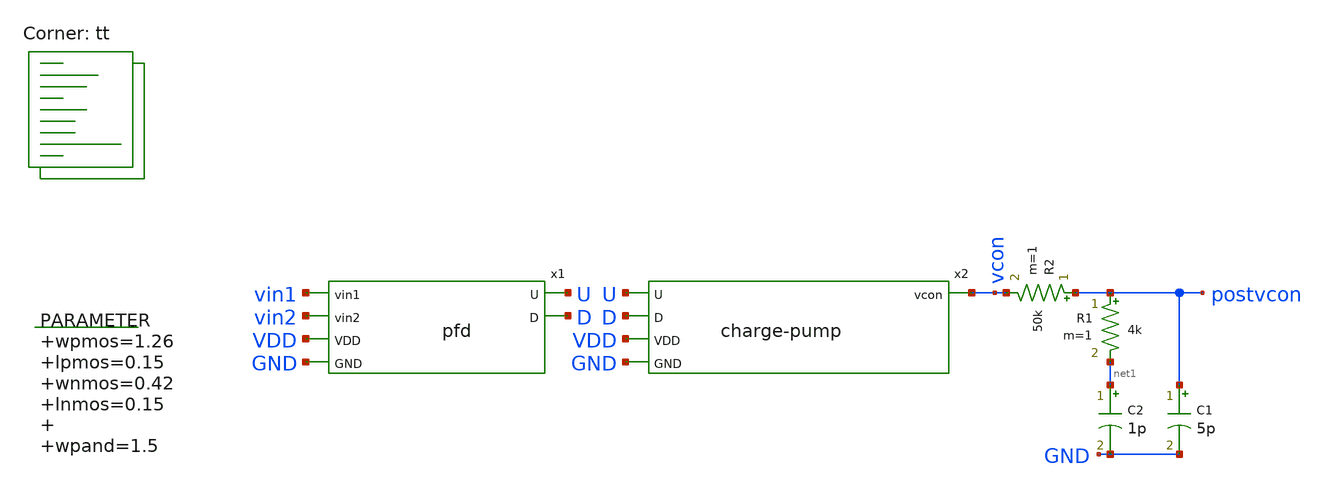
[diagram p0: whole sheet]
** sch_path: xschem/pll-tb.sch
**.subckt pll-tb
.param wpmos=1.26 lpmos=0.15 wnmos=0.42 lnmos=0.15 wpand=1.5

x2 U D vcon VDD GND charge-pump
x1 vin1 vin2 U D VDD GND pfd
C2 net1 GND 1p m=1
R1 postvcon net1 4k m=1
R2 postvcon vcon 50k m=1
C1 postvcon GND 5p m=1
**** begin user architecture code
 .lib $::SKYWATER_MODELS/sky130.lib.spice tt
.include $::SKYWATER_STDCELLS/sky130_fd_sc_hd.spice
.param mc_mm_switch = 0
.param mc_pr_switch = 0




  .param max_freq=120e6 period={1/max_freq} time_high={period/2}
  .param delay_vin1={time_high} delay_vin2={time_high*1.5}

  .option wnflag=1
  .option safecurrents

  Vvdd vdd  gnd 1.8
  Vin1 vin1 gnd pulse(0 1.8 {delay_vin1} 1p 1p {time_high} {period})
  Vin2 vin2 gnd pulse(0 1.8 {delay_vin2} 1p 1p {time_high} {period})

  .control
     reset
     save all
     tran 0.01n 2u
     write pll-tb.raw
     *set appendwrite

     *1=0 1.5=90 2=180 3=360
     *let phase=1

     *while phase <= 2
      *alter @vin2[PULSE] [ 0 1.8 {delay_vin2*$&phase} 1p 1p {time_high} {period}) ]
      *reset
      *save all
      *tran 0.01n 300n
      *write pll-tb.raw
      *let phase = phase + 0.25
     *end
    quit 0
  .endc



**** end user architecture code
**.ends

* expanding   symbol:  charge-pump.sym # of pins=5
** sym_path: xschem/charge-pump.sym
** sch_path: xschem/charge-pump.sch
.subckt charge-pump U D vcon VDD GND
*.ipin U
*.ipin D
*.opin vcon
*.ipin VDD
*.ipin GND
XM1 vcon Ub VDD VDD sky130_fd_pr__pfet_01v8 L=0.36 W=4.8 nf=1 ad='int((nf+1)/2) * W/nf * 0.29' as='int((nf+2)/2) * W/nf * 0.29'
+ pd='2*int((nf+1)/2) * (W/nf + 0.29)' ps='2*int((nf+2)/2) * (W/nf + 0.29)' nrd='0.29 / W' nrs='0.29 / W'
+ sa=0 sb=0 sd=0 mult=1 m=1
XM2 vcon D GND GND sky130_fd_pr__nfet_01v8 L=0.36 W=0.96 nf=1 ad='int((nf+1)/2) * W/nf * 0.29' as='int((nf+2)/2) * W/nf * 0.29'
+ pd='2*int((nf+1)/2) * (W/nf + 0.29)' ps='2*int((nf+2)/2) * (W/nf + 0.29)' nrd='0.29 / W' nrs='0.29 / W'
+ sa=0 sb=0 sd=0 mult=1 m=1
XM3 Ub U VDD VDD sky130_fd_pr__pfet_01v8 L=0.18 W=4.8 nf=1 ad='int((nf+1)/2) * W/nf * 0.29' as='int((nf+2)/2) * W/nf * 0.29'
+ pd='2*int((nf+1)/2) * (W/nf + 0.29)' ps='2*int((nf+2)/2) * (W/nf + 0.29)' nrd='0.29 / W' nrs='0.29 / W'
+ sa=0 sb=0 sd=0 mult=1 m=1
XM4 Ub U GND GND sky130_fd_pr__nfet_01v8 L=0.18 W=1.2 nf=1 ad='int((nf+1)/2) * W/nf * 0.29' as='int((nf+2)/2) * W/nf * 0.29'
+ pd='2*int((nf+1)/2) * (W/nf + 0.29)' ps='2*int((nf+2)/2) * (W/nf + 0.29)' nrd='0.29 / W' nrs='0.29 / W'
+ sa=0 sb=0 sd=0 mult=1 m=1
.ends


* expanding   symbol:  pfd.sym # of pins=6
** sym_path: xschem/pfd.sym
** sch_path: xschem/pfd.sch
.subckt pfd vin1 vin2 U D VDD GND
*.ipin vin1
*.ipin vin2
*.opin U
*.opin D
*.ipin VDD
*.ipin GND
.param wpmos=1.26 lpmos=0.15 wnmos=0.42 lnmos=0.15 wpand=1.5

XM1 net4 rst GND GND sky130_fd_pr__nfet_01v8 L=lnmos W=wnmos nf=1 ad='int((nf+1)/2) * W/nf * 0.29' as='int((nf+2)/2) * W/nf * 0.29'
+ pd='2*int((nf+1)/2) * (W/nf + 0.29)' ps='2*int((nf+2)/2) * (W/nf + 0.29)' nrd='0.29 / W' nrs='0.29 / W'
+ sa=0 sb=0 sd=0 mult=1 m=1
XM2 net3 vin1 VDD VDD sky130_fd_pr__pfet_01v8 L=lpmos W=wpmos nf=1 ad='int((nf+1)/2) * W/nf * 0.29' as='int((nf+2)/2) * W/nf * 0.29'
+ pd='2*int((nf+1)/2) * (W/nf + 0.29)' ps='2*int((nf+2)/2) * (W/nf + 0.29)' nrd='0.29 / W' nrs='0.29 / W'
+ sa=0 sb=0 sd=0 mult=1 m=1
XM3 net4 rst net3 VDD sky130_fd_pr__pfet_01v8 L=lpmos W=wpmos nf=1 ad='int((nf+1)/2) * W/nf * 0.29' as='int((nf+2)/2) * W/nf * 0.29'
+ pd='2*int((nf+1)/2) * (W/nf + 0.29)' ps='2*int((nf+2)/2) * (W/nf + 0.29)' nrd='0.29 / W' nrs='0.29 / W'
+ sa=0 sb=0 sd=0 mult=1 m=1
XM4 net1 net4 VDD VDD sky130_fd_pr__pfet_01v8 L=lpmos W=wpmos nf=1 ad='int((nf+1)/2) * W/nf * 0.29' as='int((nf+2)/2) * W/nf * 0.29'
+ pd='2*int((nf+1)/2) * (W/nf + 0.29)' ps='2*int((nf+2)/2) * (W/nf + 0.29)' nrd='0.29 / W' nrs='0.29 / W'
+ sa=0 sb=0 sd=0 mult=1 m=1
XM5 preU net1 VDD VDD sky130_fd_pr__pfet_01v8 L=lpmos W=wpmos nf=1 ad='int((nf+1)/2) * W/nf * 0.29' as='int((nf+2)/2) * W/nf * 0.29'
+ pd='2*int((nf+1)/2) * (W/nf + 0.29)' ps='2*int((nf+2)/2) * (W/nf + 0.29)' nrd='0.29 / W' nrs='0.29 / W'
+ sa=0 sb=0 sd=0 mult=1 m=1
XM6 net1 net4 net2 GND sky130_fd_pr__nfet_01v8 L=lnmos W=wnmos nf=1 ad='int((nf+1)/2) * W/nf * 0.29'
+ as='int((nf+2)/2) * W/nf * 0.29' pd='2*int((nf+1)/2) * (W/nf + 0.29)' ps='2*int((nf+2)/2) * (W/nf + 0.29)'
+ nrd='0.29 / W' nrs='0.29 / W' sa=0 sb=0 sd=0 mult=1 m=1
XM7 preU net1 GND GND sky130_fd_pr__nfet_01v8 L=lnmos W=wnmos nf=1 ad='int((nf+1)/2) * W/nf * 0.29' as='int((nf+2)/2) * W/nf * 0.29'
+ pd='2*int((nf+1)/2) * (W/nf + 0.29)' ps='2*int((nf+2)/2) * (W/nf + 0.29)' nrd='0.29 / W' nrs='0.29 / W'
+ sa=0 sb=0 sd=0 mult=1 m=1
XM8 net2 vin1 GND GND sky130_fd_pr__nfet_01v8 L=lnmos W=wnmos nf=1 ad='int((nf+1)/2) * W/nf * 0.29' as='int((nf+2)/2) * W/nf * 0.29'
+ pd='2*int((nf+1)/2) * (W/nf + 0.29)' ps='2*int((nf+2)/2) * (W/nf + 0.29)' nrd='0.29 / W' nrs='0.29 / W'
+ sa=0 sb=0 sd=0 mult=1 m=1
XM10 net6 vin2 VDD VDD sky130_fd_pr__pfet_01v8 L=lpmos W=wpmos nf=1 ad='int((nf+1)/2) * W/nf * 0.29'
+ as='int((nf+2)/2) * W/nf * 0.29' pd='2*int((nf+1)/2) * (W/nf + 0.29)' ps='2*int((nf+2)/2) * (W/nf + 0.29)'
+ nrd='0.29 / W' nrs='0.29 / W' sa=0 sb=0 sd=0 mult=1 m=1
XM11 net5 net7 VDD VDD sky130_fd_pr__pfet_01v8 L=lpmos W=wpmos nf=1 ad='int((nf+1)/2) * W/nf * 0.29'
+ as='int((nf+2)/2) * W/nf * 0.29' pd='2*int((nf+1)/2) * (W/nf + 0.29)' ps='2*int((nf+2)/2) * (W/nf + 0.29)'
+ nrd='0.29 / W' nrs='0.29 / W' sa=0 sb=0 sd=0 mult=1 m=1
XM12 net7 rst net6 VDD sky130_fd_pr__pfet_01v8 L=lpmos W=wpmos nf=1 ad='int((nf+1)/2) * W/nf * 0.29'
+ as='int((nf+2)/2) * W/nf * 0.29' pd='2*int((nf+1)/2) * (W/nf + 0.29)' ps='2*int((nf+2)/2) * (W/nf + 0.29)'
+ nrd='0.29 / W' nrs='0.29 / W' sa=0 sb=0 sd=0 mult=1 m=1
XM13 preD net5 VDD VDD sky130_fd_pr__pfet_01v8 L=lpmos W=wpmos nf=1 ad='int((nf+1)/2) * W/nf * 0.29'
+ as='int((nf+2)/2) * W/nf * 0.29' pd='2*int((nf+1)/2) * (W/nf + 0.29)' ps='2*int((nf+2)/2) * (W/nf + 0.29)'
+ nrd='0.29 / W' nrs='0.29 / W' sa=0 sb=0 sd=0 mult=1 m=1
XM14 net7 rst GND GND sky130_fd_pr__nfet_01v8 L=lnmos W=wnmos nf=1 ad='int((nf+1)/2) * W/nf * 0.29' as='int((nf+2)/2) * W/nf * 0.29'
+ pd='2*int((nf+1)/2) * (W/nf + 0.29)' ps='2*int((nf+2)/2) * (W/nf + 0.29)' nrd='0.29 / W' nrs='0.29 / W'
+ sa=0 sb=0 sd=0 mult=1 m=1
XM15 net5 net7 net8 GND sky130_fd_pr__nfet_01v8 L=lnmos W=wnmos nf=1 ad='int((nf+1)/2) * W/nf * 0.29'
+ as='int((nf+2)/2) * W/nf * 0.29' pd='2*int((nf+1)/2) * (W/nf + 0.29)' ps='2*int((nf+2)/2) * (W/nf + 0.29)'
+ nrd='0.29 / W' nrs='0.29 / W' sa=0 sb=0 sd=0 mult=1 m=1
XM16 preD net5 GND GND sky130_fd_pr__nfet_01v8 L=lnmos W=wnmos nf=1 ad='int((nf+1)/2) * W/nf * 0.29'
+ as='int((nf+2)/2) * W/nf * 0.29' pd='2*int((nf+1)/2) * (W/nf + 0.29)' ps='2*int((nf+2)/2) * (W/nf + 0.29)'
+ nrd='0.29 / W' nrs='0.29 / W' sa=0 sb=0 sd=0 mult=1 m=1
XM18 net8 vin2 GND GND sky130_fd_pr__nfet_01v8 L=lnmos W=wnmos nf=1 ad='int((nf+1)/2) * W/nf * 0.29'
+ as='int((nf+2)/2) * W/nf * 0.29' pd='2*int((nf+1)/2) * (W/nf + 0.29)' ps='2*int((nf+2)/2) * (W/nf + 0.29)'
+ nrd='0.29 / W' nrs='0.29 / W' sa=0 sb=0 sd=0 mult=1 m=1
x1 preU GND GND VDD VDD U sky130_fd_sc_hd__buf_8
x2 preD GND GND VDD VDD D sky130_fd_sc_hd__buf_8
x3 prerst GND GND VDD VDD rst sky130_fd_sc_hd__buf_1
x4 U D GND GND VDD VDD prerst sky130_fd_sc_hd__and2_1
.ends

.end
